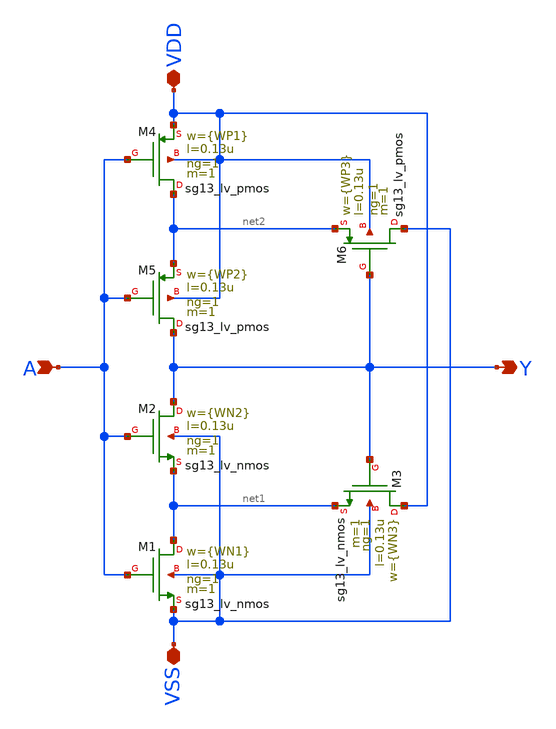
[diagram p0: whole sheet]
** sch_path: xschem/strig.sch
**.subckt strig VDD VSS A Y
*.iopin VDD
*.iopin VSS
*.ipin A
*.opin Y
XM1 net1 A VSS VSS sg13_lv_nmos w={WN1} l=0.13u ng=1 m=1 mm_ok=1
XM2 Y A net1 VSS sg13_lv_nmos w={WN2} l=0.13u ng=1 m=1 mm_ok=1
XM3 VDD Y net1 VSS sg13_lv_nmos w={WN3} l=0.13u ng=1 m=1 mm_ok=1
XM6 VSS Y net2 VDD sg13_lv_pmos w={WP3} l=0.13u ng=1 m=1 mm_ok=1
XM5 Y A net2 VDD sg13_lv_pmos w={WP2} l=0.13u ng=1 m=1 mm_ok=1
XM4 net2 A VDD VDD sg13_lv_pmos w={WP1} l=0.13u ng=1 m=1 mm_ok=1
**.ends
.end
